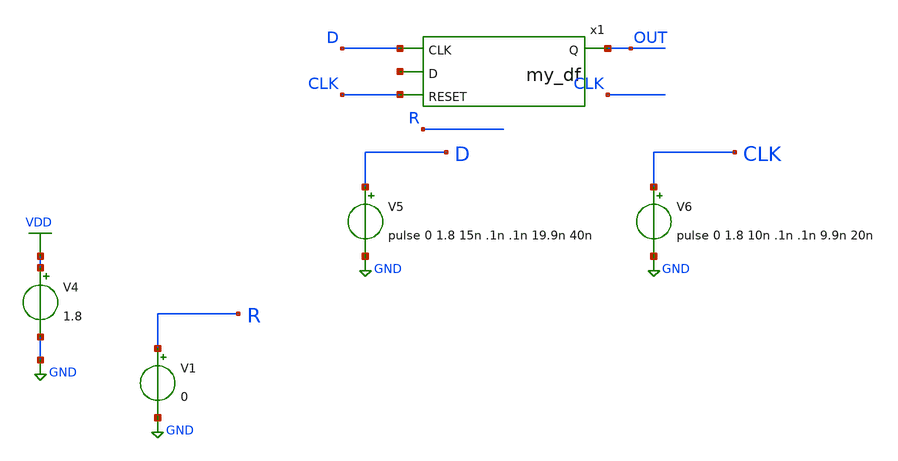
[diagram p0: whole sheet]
** sch_path: tb_df.sch
**.subckt tb_df
V4 VDD GND 1.8
V5 D GND pulse 0 1.8 15n .1n .1n 19.9n 40n
V6 CLK GND pulse 0 1.8 10n .1n .1n 9.9n 20n
V1 R GND 0
x1 D OUT net1 CLK my_df
**** begin user architecture code
 .lib $::SKYWATER_MODELS/sky130.lib.spice tt
.include $::SKYWATER_STDCELLS/sky130_fd_sc_hd.spice



.options acct list
.temp 25

.tran 1n 0.1u
.control
.write tb_saradc.raw
.endc


**** end user architecture code
**.ends

* expanding   symbol:  my_df.sym # of pins=4
** sym_path: my_df.sym
** sch_path: my_df.sch
.subckt my_df CLK Q D RESET
*.ipin CLK
*.ipin D
*.ipin RESET
*.opin Q
x1 RESET GND GND VDD VDD net1 sky130_fd_sc_hd__inv_1
x2 CLK D net1 VDD GND GND VDD VDD Q GND sky130_fd_sc_hd__dfbbp_1
.ends

.GLOBAL VDD
.GLOBAL GND
.end
